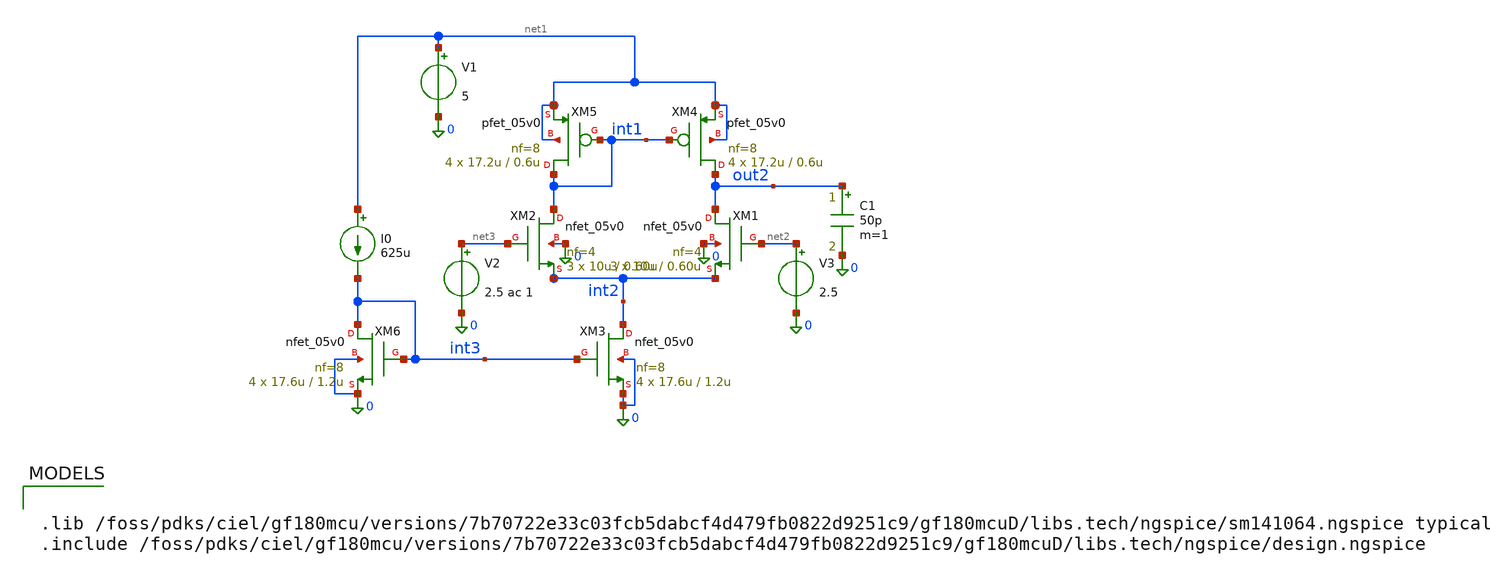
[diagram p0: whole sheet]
** sch_path: gm3_ota_tb.sch
**.subckt gm3_ota_tb
XM1 out2 net2 int2 0 nfet_05v0 L=0.60u W=10u nf=4 ad='int((nf+1)/2) * W/nf * 0.18u' as='int((nf+2)/2) * W/nf * 0.18u'
+ pd='2*int((nf+1)/2) * (W/nf + 0.18u)' ps='2*int((nf+2)/2) * (W/nf + 0.18u)' nrd='0.18u / W' nrs='0.18u / W'
+ sa=0 sb=0 sd=0 m=3
XM3 int2 int3 0 0 nfet_05v0 L=1.2u W=17.6u nf=8 ad='int((nf+1)/2) * W/nf * 0.18u' as='int((nf+2)/2) * W/nf * 0.18u'
+ pd='2*int((nf+1)/2) * (W/nf + 0.18u)' ps='2*int((nf+2)/2) * (W/nf + 0.18u)' nrd='0.18u / W' nrs='0.18u / W'
+ sa=0 sb=0 sd=0 m=4
XM4 out2 int1 net1 net1 pfet_05v0 L=0.6u W=17.2u nf=8 ad='int((nf+1)/2) * W/nf * 0.18u' as='int((nf+2)/2) * W/nf * 0.18u'
+ pd='2*int((nf+1)/2) * (W/nf + 0.18u)' ps='2*int((nf+2)/2) * (W/nf + 0.18u)' nrd='0.18u / W' nrs='0.18u / W'
+ sa=0 sb=0 sd=0 m=4
V1 net1 0 5
V2 net3 0 2.5 ac 1
V3 net2 0 2.5
C1 out2 0 50p m=1
I0 net1 int3 625u
XM6 int3 int3 0 0 nfet_05v0 L=1.2u W=17.6u nf=8 ad='int((nf+1)/2) * W/nf * 0.18u' as='int((nf+2)/2) * W/nf * 0.18u'
+ pd='2*int((nf+1)/2) * (W/nf + 0.18u)' ps='2*int((nf+2)/2) * (W/nf + 0.18u)' nrd='0.18u / W' nrs='0.18u / W'
+ sa=0 sb=0 sd=0 m=4
XM2 int1 net3 int2 0 nfet_05v0 L=0.60u W=10u nf=4 ad='int((nf+1)/2) * W/nf * 0.18u' as='int((nf+2)/2) * W/nf * 0.18u'
+ pd='2*int((nf+1)/2) * (W/nf + 0.18u)' ps='2*int((nf+2)/2) * (W/nf + 0.18u)' nrd='0.18u / W' nrs='0.18u / W'
+ sa=0 sb=0 sd=0 m=3
XM5 int1 int1 net1 net1 pfet_05v0 L=0.6u W=17.2u nf=8 ad='int((nf+1)/2) * W/nf * 0.18u' as='int((nf+2)/2) * W/nf * 0.18u'
+ pd='2*int((nf+1)/2) * (W/nf + 0.18u)' ps='2*int((nf+2)/2) * (W/nf + 0.18u)' nrd='0.18u / W' nrs='0.18u / W'
+ sa=0 sb=0 sd=0 m=4
**** begin user architecture code


.lib /foss/pdks/ciel/gf180mcu/versions/7b70722e33c03fcb5dabcf4d479fb0822d9251c9/gf180mcuD/libs.tech/ngspice/sm141064.ngspice typical
.include /foss/pdks/ciel/gf180mcu/versions/7b70722e33c03fcb5dabcf4d479fb0822d9251c9/gf180mcuD/libs.tech/ngspice/design.ngspice




.control
  	save all
	op
	ac dec 20 1 100Meg
	remzerovec
	write gm3_OTA_ac.raw
.endc

.options savecurrents


**** end user architecture code
**.ends
.end
